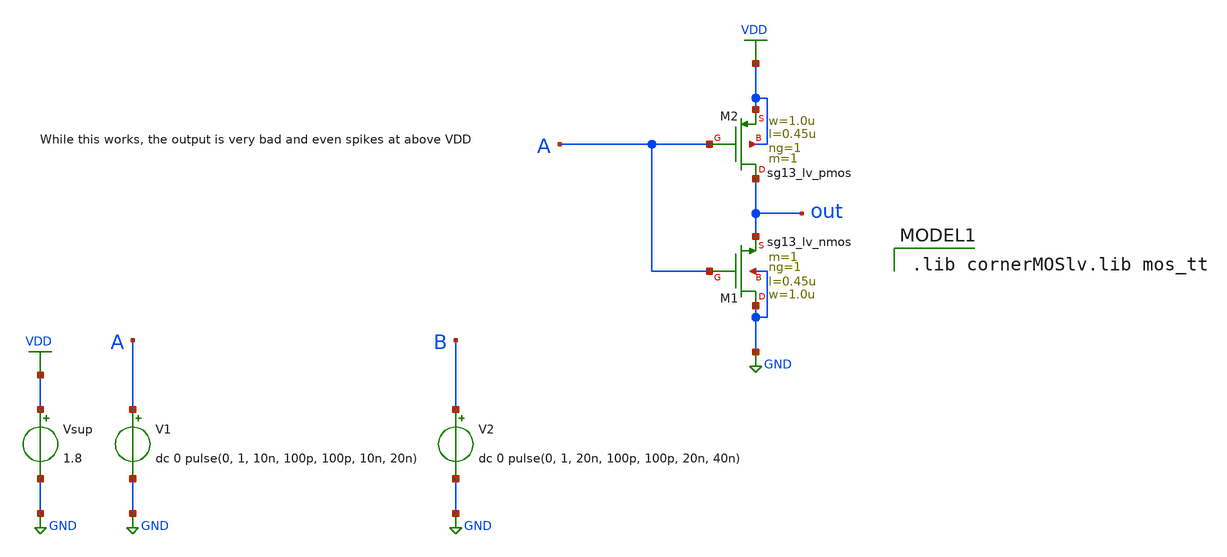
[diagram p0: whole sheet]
** sch_path: design/design_clkgen/inverter/basic_inv.sch
**.subckt basic_inv
XM1 GND A out GND sg13_lv_nmos w=1.0u l=0.45u ng=1 m=1 mm_ok=1
V1 A GND dc 0 pulse(0, 1, 10n, 100p, 100p, 10n, 20n)
V2 B GND dc 0 pulse(0, 1, 20n, 100p, 100p, 20n, 40n)
Vsup VDD GND 1.8
XM2 out A VDD VDD sg13_lv_pmos w=1.0u l=0.45u ng=1 m=1 mm_ok=1
**** begin user architecture code


.tran 10p 100n
.save all


 .lib cornerMOSlv.lib mos_tt

**** end user architecture code
**.ends
.GLOBAL GND
.GLOBAL VDD
.end
